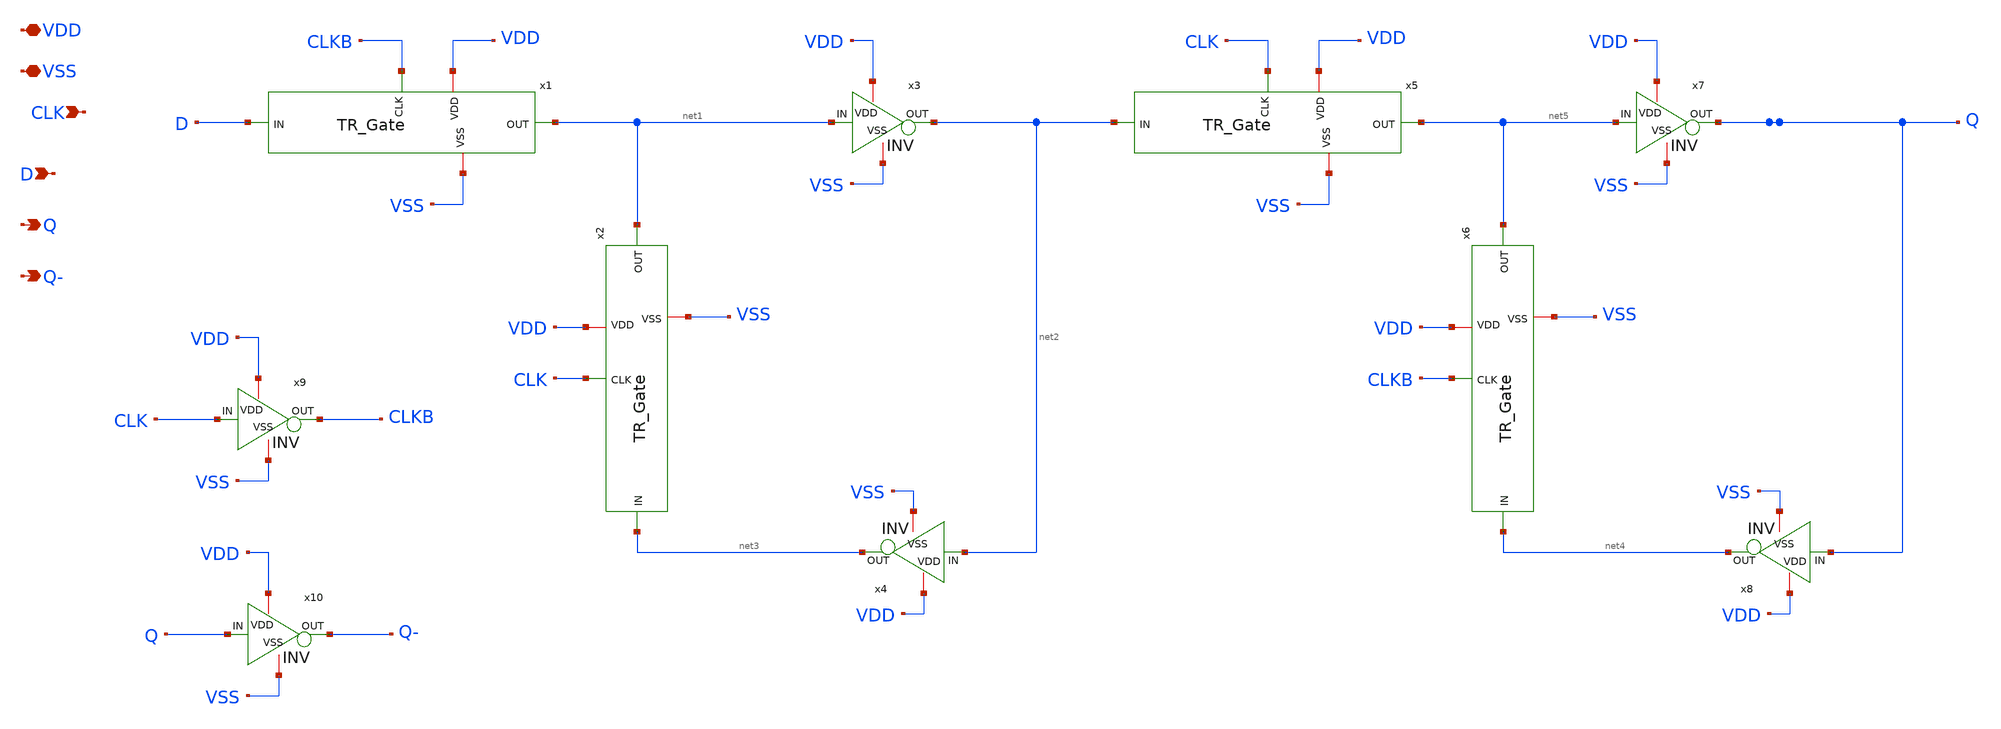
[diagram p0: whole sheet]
** sch_path: Xschem/PLL_TOP_Schematics/D-FF.sch
**.subckt D-FF VDD VSS CLK D Q Q-
*.iopin VDD
*.iopin VSS
*.ipin CLK
*.ipin D
*.opin Q
*.opin Q-
x1 net1 VDD VSS D CLKB TR_Gate
x2 net1 VDD VSS net3 CLK TR_Gate
x3 VSS VDD net2 net1 INV
x4 VSS VDD net3 net2 INV
x5 net5 VDD VSS net2 CLK TR_Gate
x6 net5 VDD VSS net4 CLKB TR_Gate
x8 VSS VDD net4 Q INV
x9 VSS VDD CLKB CLK INV
x10 VSS VDD Q- Q INV
x7 VSS VDD Q net5 INV
**.ends

* expanding   symbol:  TR_Gate.sym # of pins=5
** sym_path: Xschem/PLL_TOP_Schematics/TR_Gate.sym
** sch_path: Xschem/PLL_TOP_Schematics/TR_Gate.sch
.subckt TR_Gate OUT VDD VSS IN CLK
*.iopin VDD
*.iopin VSS
*.ipin IN
*.opin OUT
*.ipin CLK
XM2 net1 CLK VDD VDD sky130_fd_pr__pfet_01v8 L=0.2 W=5 nf=1 ad='int((nf+1)/2) * W/nf * 0.29' as='int((nf+2)/2) * W/nf * 0.29'
+ pd='2*int((nf+1)/2) * (W/nf + 0.29)' ps='2*int((nf+2)/2) * (W/nf + 0.29)' nrd='0.29 / W' nrs='0.29 / W'
+ sa=0 sb=0 sd=0 mult=1 m=1
XM3 IN net1 OUT VDD sky130_fd_pr__pfet_01v8 L=0.2 W=8 nf=1 ad='int((nf+1)/2) * W/nf * 0.29' as='int((nf+2)/2) * W/nf * 0.29'
+ pd='2*int((nf+1)/2) * (W/nf + 0.29)' ps='2*int((nf+2)/2) * (W/nf + 0.29)' nrd='0.29 / W' nrs='0.29 / W'
+ sa=0 sb=0 sd=0 mult=1 m=1
XM4 net1 CLK VSS VSS sky130_fd_pr__nfet_01v8 L=0.2 W=2.5 nf=1 ad='int((nf+1)/2) * W/nf * 0.29' as='int((nf+2)/2) * W/nf * 0.29'
+ pd='2*int((nf+1)/2) * (W/nf + 0.29)' ps='2*int((nf+2)/2) * (W/nf + 0.29)' nrd='0.29 / W' nrs='0.29 / W'
+ sa=0 sb=0 sd=0 mult=1 m=1
XM5 IN CLK OUT VSS sky130_fd_pr__nfet_01v8 L=0.2 W=8 nf=1 ad='int((nf+1)/2) * W/nf * 0.29' as='int((nf+2)/2) * W/nf * 0.29'
+ pd='2*int((nf+1)/2) * (W/nf + 0.29)' ps='2*int((nf+2)/2) * (W/nf + 0.29)' nrd='0.29 / W' nrs='0.29 / W'
+ sa=0 sb=0 sd=0 mult=1 m=1
.ends


* expanding   symbol:  INV.sym # of pins=4
** sym_path: Xschem/PLL_TOP_Schematics/INV.sym
** sch_path: Xschem/PLL_TOP_Schematics/INV.sch
.subckt INV VSS VDD OUT IN
*.iopin VDD
*.iopin VSS
*.ipin IN
*.opin OUT
XM2 OUT IN VDD VDD sky130_fd_pr__pfet_01v8 L=0.2 W=6 nf=1 ad='int((nf+1)/2) * W/nf * 0.29' as='int((nf+2)/2) * W/nf * 0.29'
+ pd='2*int((nf+1)/2) * (W/nf + 0.29)' ps='2*int((nf+2)/2) * (W/nf + 0.29)' nrd='0.29 / W' nrs='0.29 / W'
+ sa=0 sb=0 sd=0 mult=1 m=1
XM4 OUT IN VSS VSS sky130_fd_pr__nfet_01v8 L=0.2 W=3 nf=1 ad='int((nf+1)/2) * W/nf * 0.29' as='int((nf+2)/2) * W/nf * 0.29'
+ pd='2*int((nf+1)/2) * (W/nf + 0.29)' ps='2*int((nf+2)/2) * (W/nf + 0.29)' nrd='0.29 / W' nrs='0.29 / W'
+ sa=0 sb=0 sd=0 mult=1 m=1
.ends

.end
